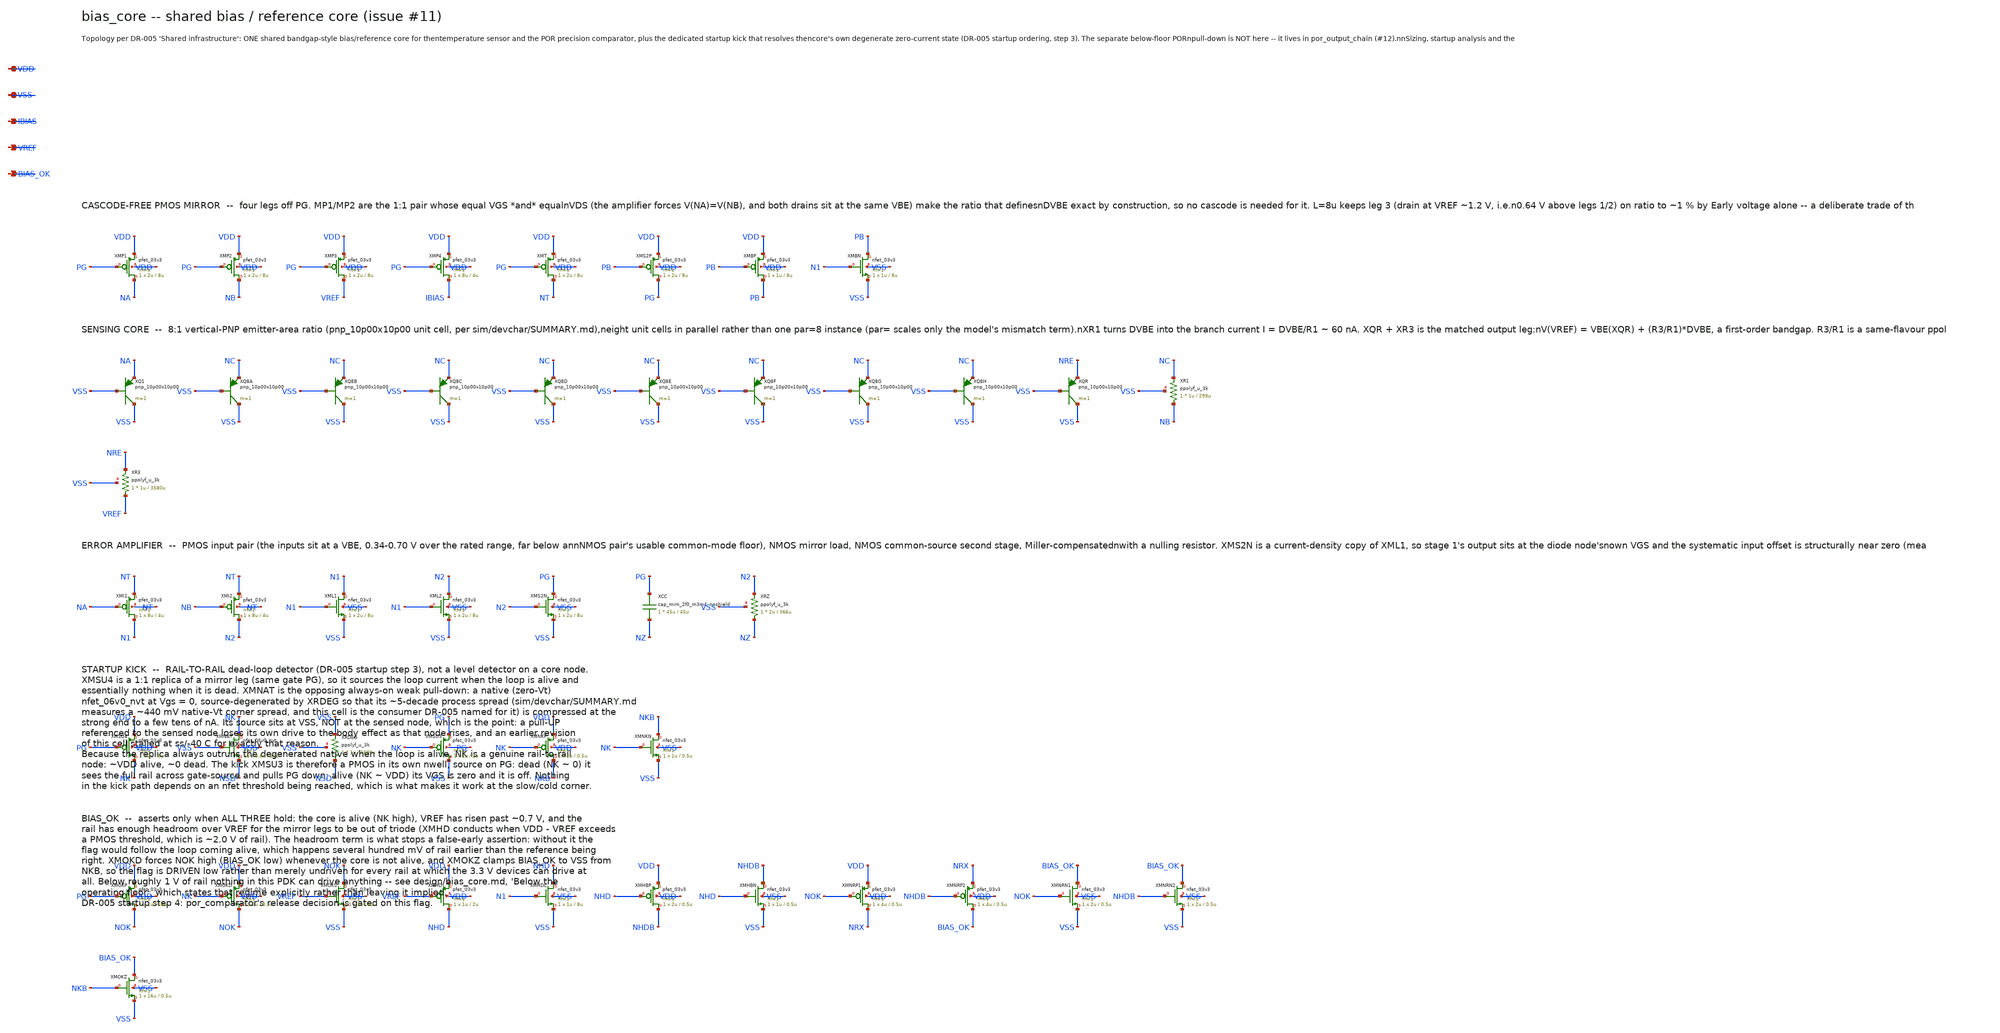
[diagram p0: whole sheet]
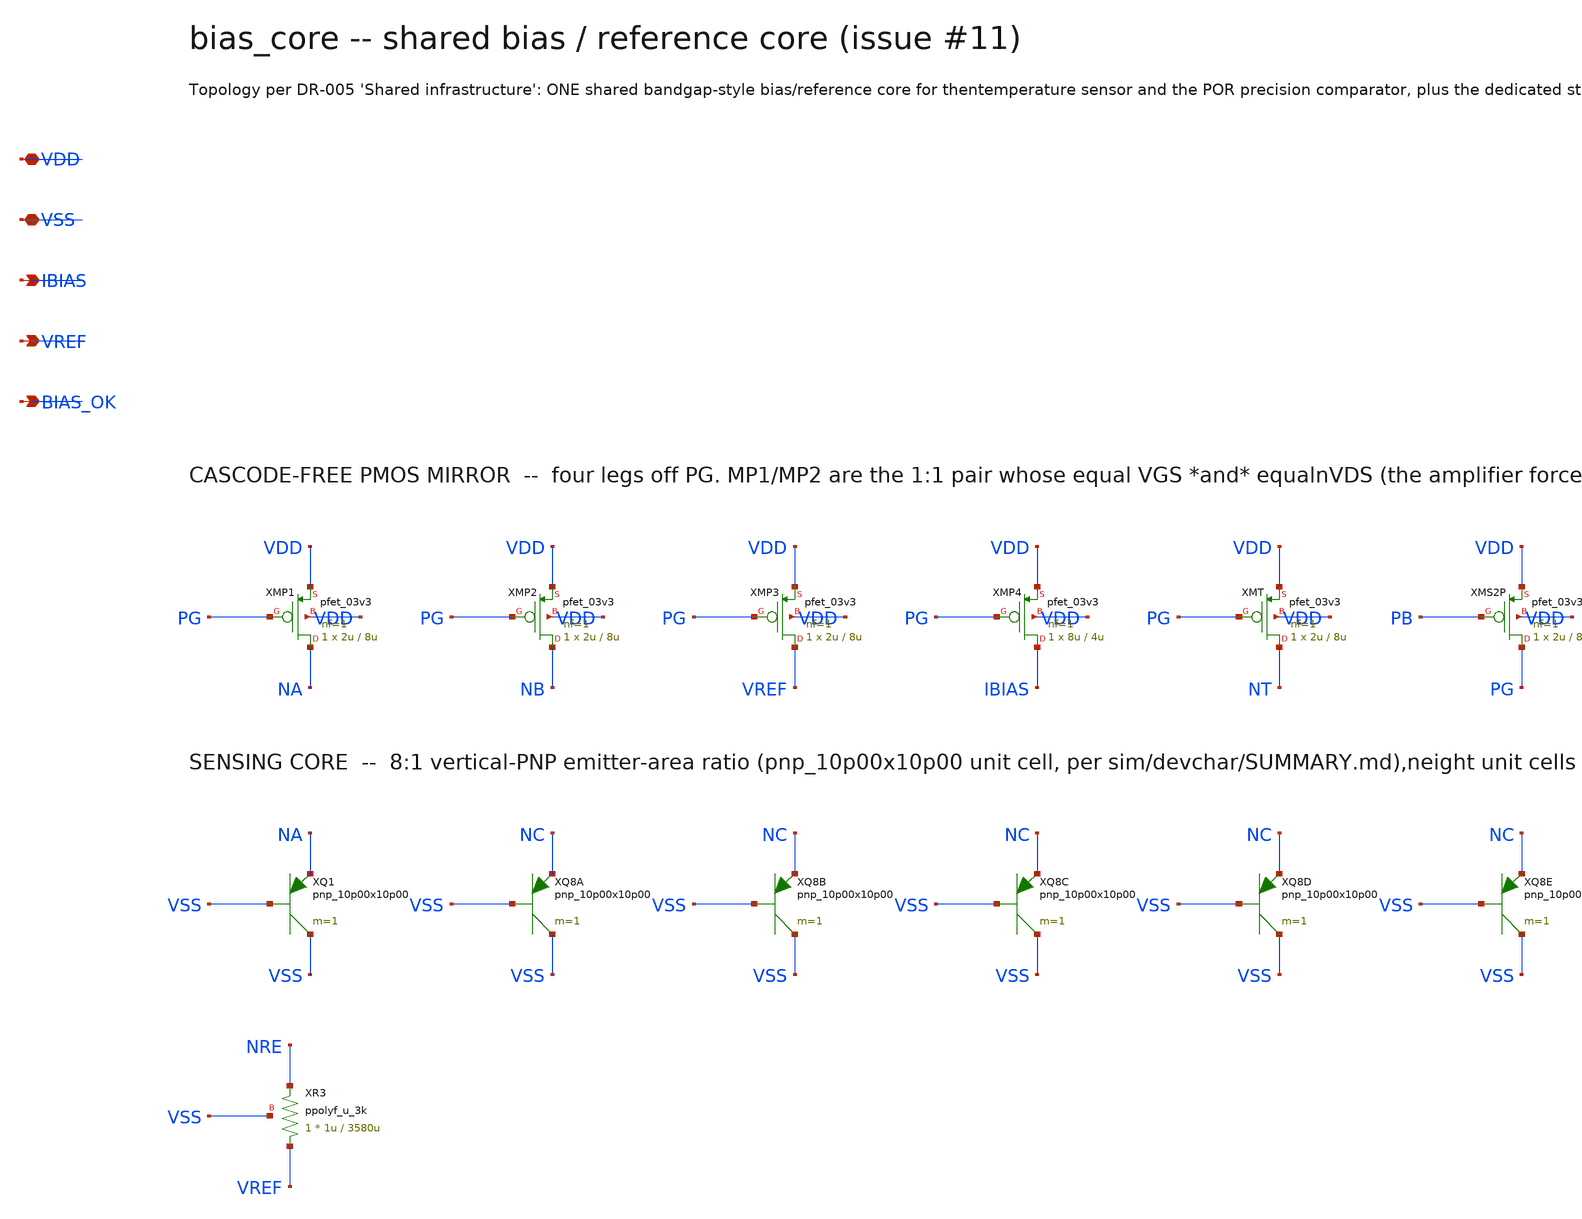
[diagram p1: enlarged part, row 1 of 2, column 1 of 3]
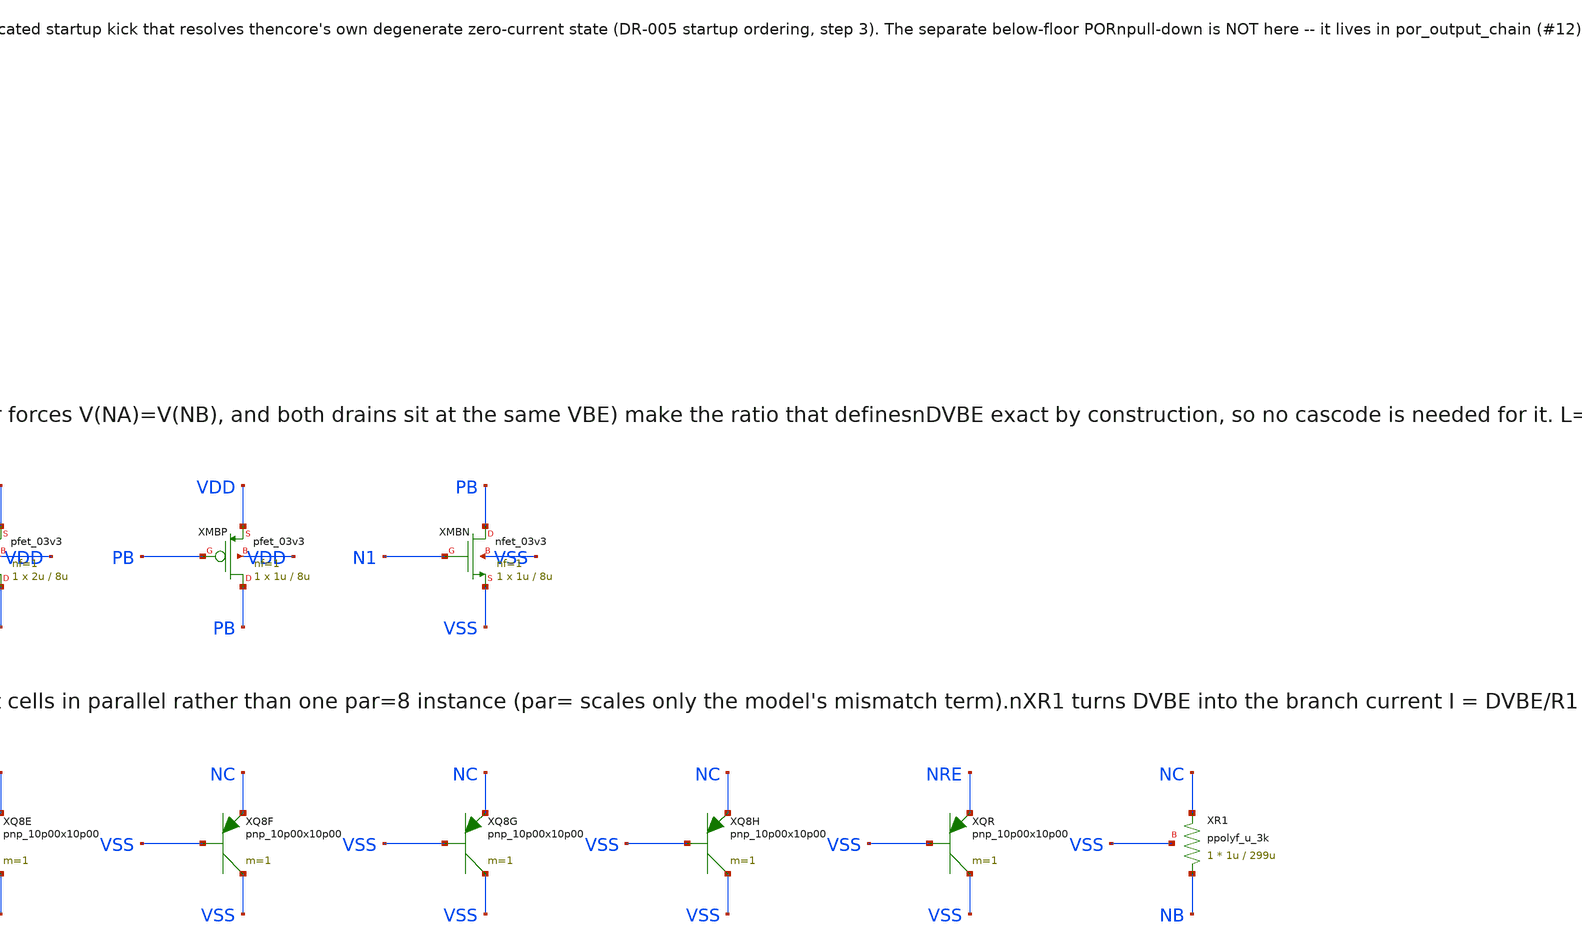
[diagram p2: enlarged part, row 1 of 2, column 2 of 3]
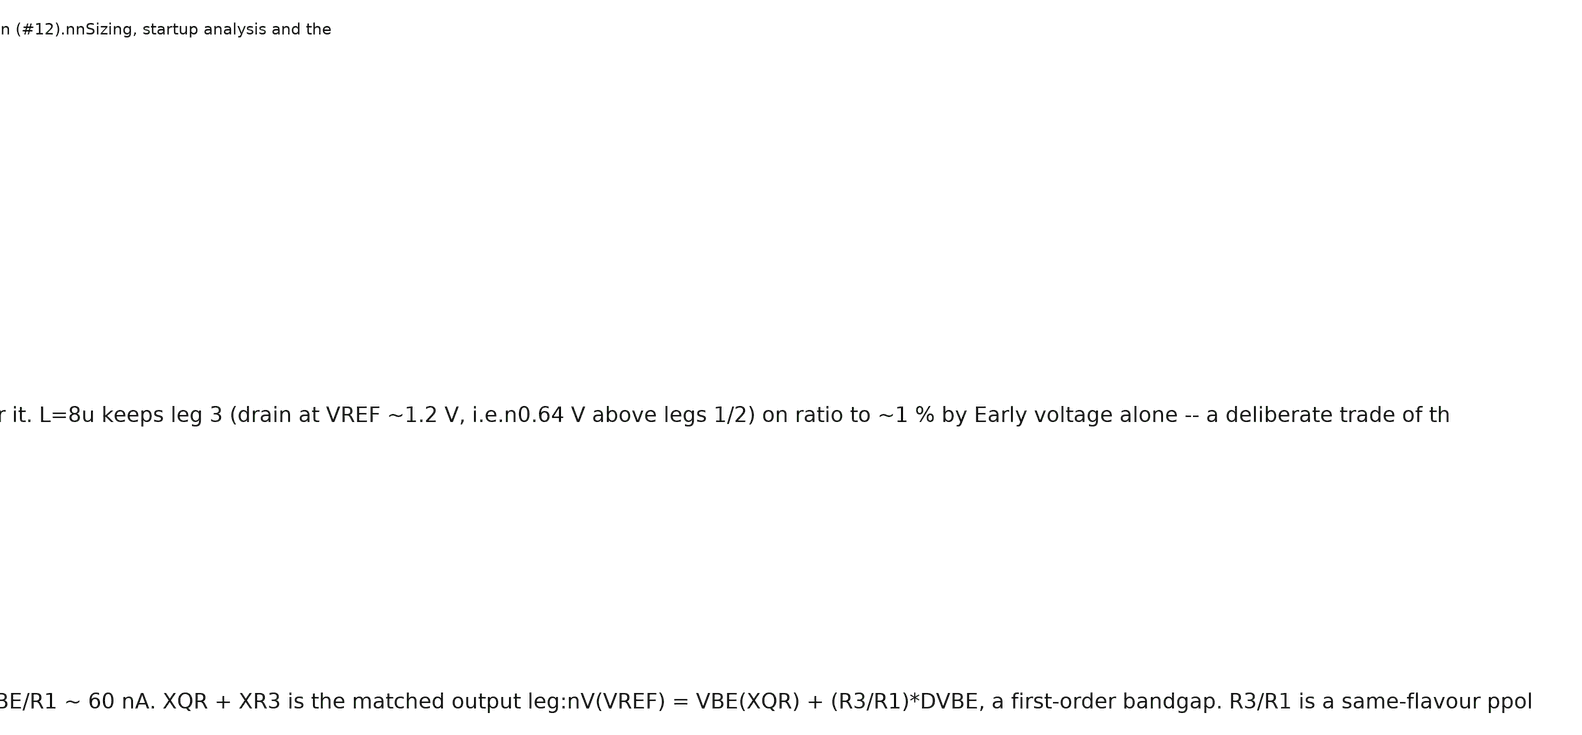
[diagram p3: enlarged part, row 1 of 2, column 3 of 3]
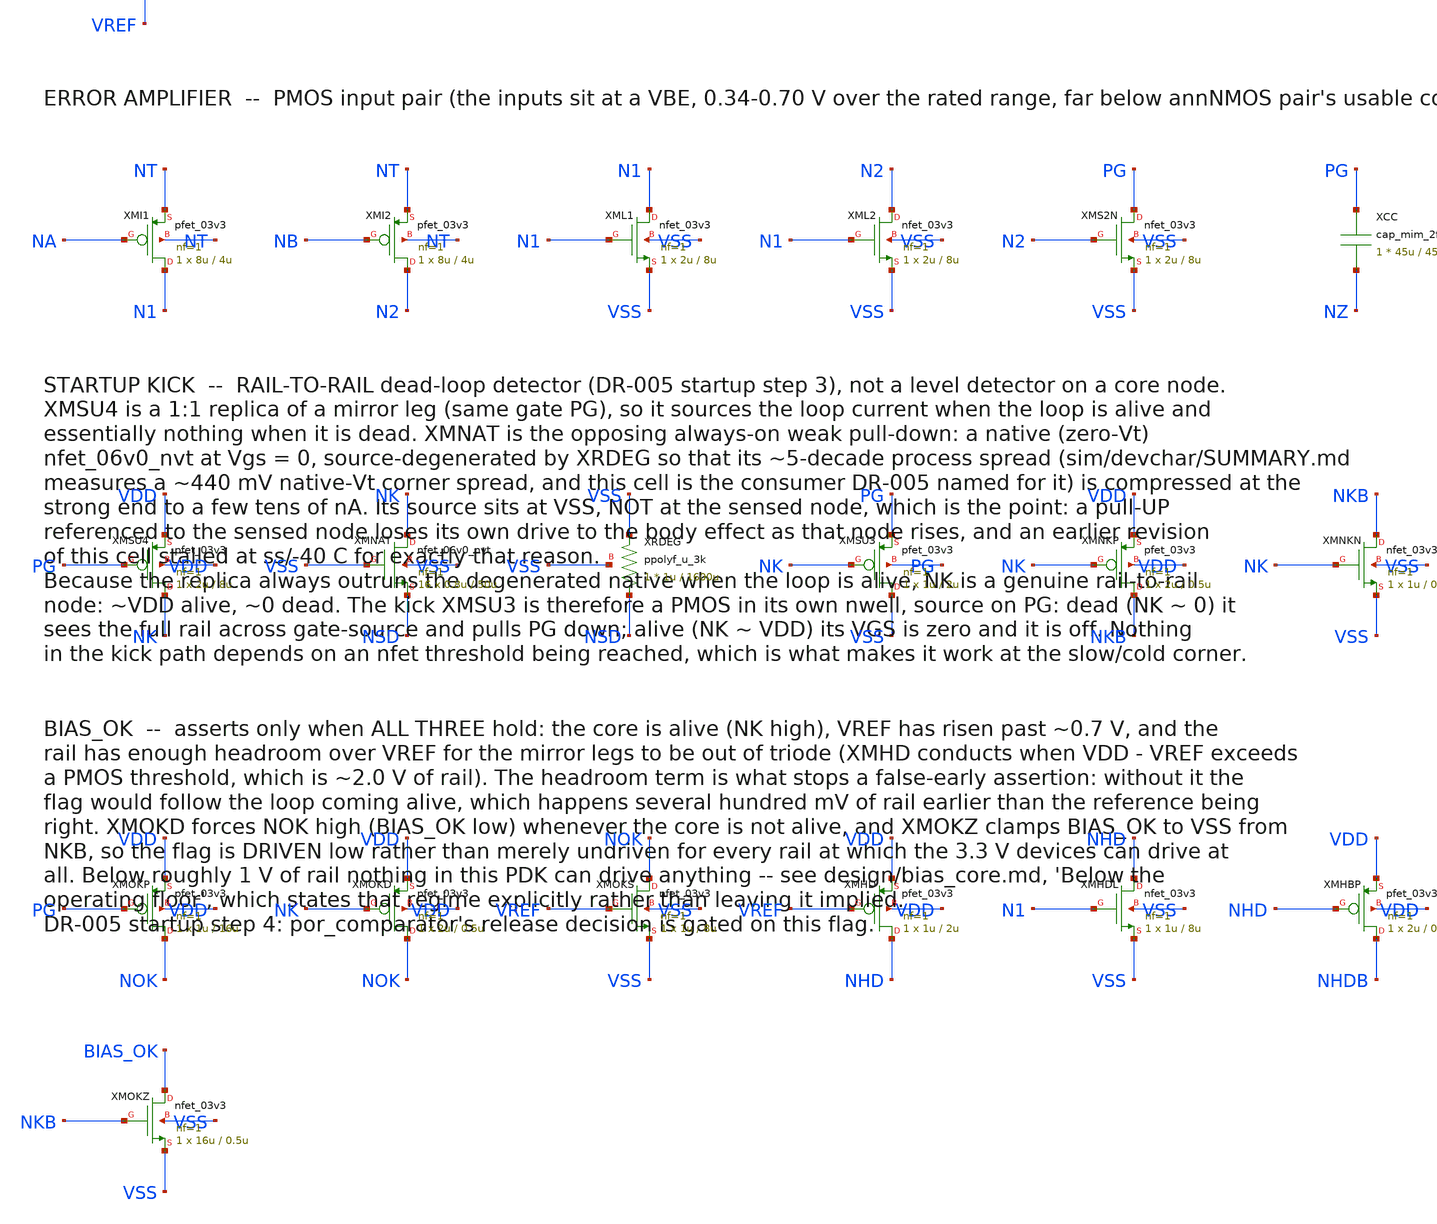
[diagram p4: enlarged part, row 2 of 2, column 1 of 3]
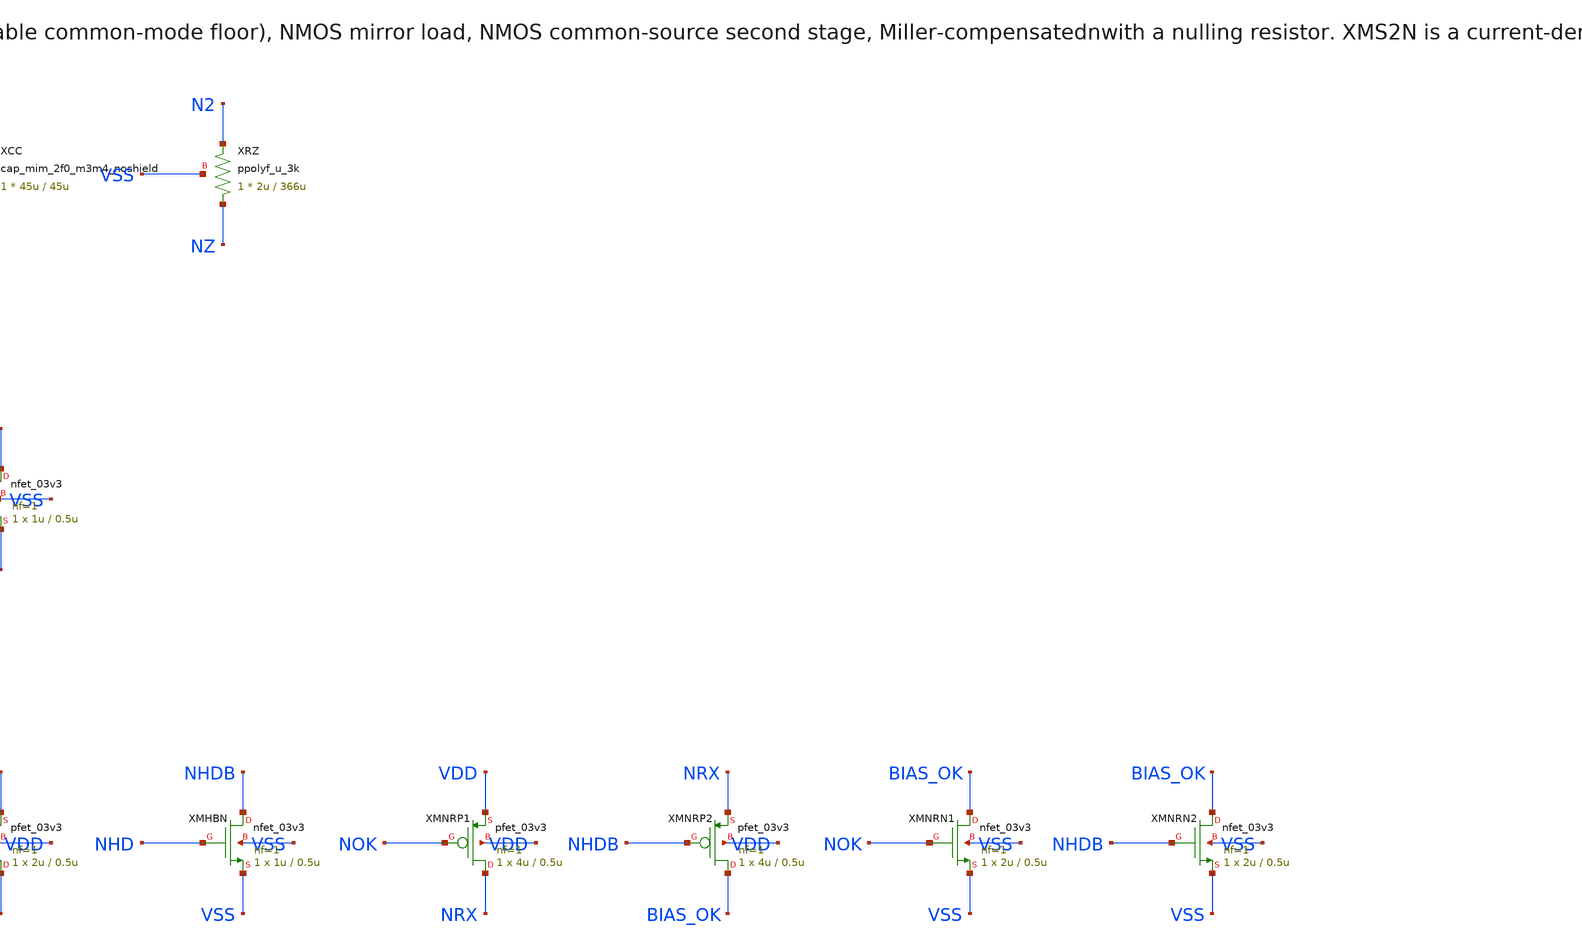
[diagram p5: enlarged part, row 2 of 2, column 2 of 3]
** sch_path: design/bias_core.sch
**.subckt bias_core VDD VSS IBIAS VREF BIAS_OK
*.iopin VDD
*.iopin VSS
*.opin IBIAS
*.opin VREF
*.opin BIAS_OK
XMP1 NA PG VDD VDD pfet_03v3 L=8u W=2u nf=1 ad='int((nf+1)/2) * W/nf * 0.18u' as='int((nf+2)/2) * W/nf * 0.18u'
+ pd='2*int((nf+1)/2) * (W/nf + 0.18u)' ps='2*int((nf+2)/2) * (W/nf + 0.18u)' nrd='0.18u / W' nrs='0.18u / W'
+ sa=0 sb=0 sd=0 m=1
XMP2 NB PG VDD VDD pfet_03v3 L=8u W=2u nf=1 ad='int((nf+1)/2) * W/nf * 0.18u' as='int((nf+2)/2) * W/nf * 0.18u'
+ pd='2*int((nf+1)/2) * (W/nf + 0.18u)' ps='2*int((nf+2)/2) * (W/nf + 0.18u)' nrd='0.18u / W' nrs='0.18u / W'
+ sa=0 sb=0 sd=0 m=1
XMP3 VREF PG VDD VDD pfet_03v3 L=8u W=2u nf=1 ad='int((nf+1)/2) * W/nf * 0.18u' as='int((nf+2)/2) * W/nf * 0.18u'
+ pd='2*int((nf+1)/2) * (W/nf + 0.18u)' ps='2*int((nf+2)/2) * (W/nf + 0.18u)' nrd='0.18u / W' nrs='0.18u / W'
+ sa=0 sb=0 sd=0 m=1
XMP4 IBIAS PG VDD VDD pfet_03v3 L=4u W=8u nf=1 ad='int((nf+1)/2) * W/nf * 0.18u' as='int((nf+2)/2) * W/nf * 0.18u'
+ pd='2*int((nf+1)/2) * (W/nf + 0.18u)' ps='2*int((nf+2)/2) * (W/nf + 0.18u)' nrd='0.18u / W' nrs='0.18u / W'
+ sa=0 sb=0 sd=0 m=1
XMT NT PG VDD VDD pfet_03v3 L=8u W=2u nf=1 ad='int((nf+1)/2) * W/nf * 0.18u' as='int((nf+2)/2) * W/nf * 0.18u'
+ pd='2*int((nf+1)/2) * (W/nf + 0.18u)' ps='2*int((nf+2)/2) * (W/nf + 0.18u)' nrd='0.18u / W' nrs='0.18u / W'
+ sa=0 sb=0 sd=0 m=1
XMS2P PG PB VDD VDD pfet_03v3 L=8u W=2u nf=1 ad='int((nf+1)/2) * W/nf * 0.18u' as='int((nf+2)/2) * W/nf * 0.18u'
+ pd='2*int((nf+1)/2) * (W/nf + 0.18u)' ps='2*int((nf+2)/2) * (W/nf + 0.18u)' nrd='0.18u / W' nrs='0.18u / W'
+ sa=0 sb=0 sd=0 m=1
XMBP PB PB VDD VDD pfet_03v3 L=8u W=1u nf=1 ad='int((nf+1)/2) * W/nf * 0.18u' as='int((nf+2)/2) * W/nf * 0.18u'
+ pd='2*int((nf+1)/2) * (W/nf + 0.18u)' ps='2*int((nf+2)/2) * (W/nf + 0.18u)' nrd='0.18u / W' nrs='0.18u / W'
+ sa=0 sb=0 sd=0 m=1
XMBN PB N1 VSS VSS nfet_03v3 L=8u W=1u nf=1 ad='int((nf+1)/2) * W/nf * 0.18u' as='int((nf+2)/2) * W/nf * 0.18u'
+ pd='2*int((nf+1)/2) * (W/nf + 0.18u)' ps='2*int((nf+2)/2) * (W/nf + 0.18u)' nrd='0.18u / W' nrs='0.18u / W'
+ sa=0 sb=0 sd=0 m=1
XQ1 VSS VSS NA pnp_10p00x10p00 m=1
XQ8A VSS VSS NC pnp_10p00x10p00 m=1
XQ8B VSS VSS NC pnp_10p00x10p00 m=1
XQ8C VSS VSS NC pnp_10p00x10p00 m=1
XQ8D VSS VSS NC pnp_10p00x10p00 m=1
XQ8E VSS VSS NC pnp_10p00x10p00 m=1
XQ8F VSS VSS NC pnp_10p00x10p00 m=1
XQ8G VSS VSS NC pnp_10p00x10p00 m=1
XQ8H VSS VSS NC pnp_10p00x10p00 m=1
XQR VSS VSS NRE pnp_10p00x10p00 m=1
XR1 NB NC VSS ppolyf_u_3k r_width=1u r_length=299u m=1
XR3 VREF NRE VSS ppolyf_u_3k r_width=1u r_length=3580u m=1
XMI1 N1 NA NT NT pfet_03v3 L=4u W=8u nf=1 ad='int((nf+1)/2) * W/nf * 0.18u' as='int((nf+2)/2) * W/nf * 0.18u'
+ pd='2*int((nf+1)/2) * (W/nf + 0.18u)' ps='2*int((nf+2)/2) * (W/nf + 0.18u)' nrd='0.18u / W' nrs='0.18u / W'
+ sa=0 sb=0 sd=0 m=1
XMI2 N2 NB NT NT pfet_03v3 L=4u W=8u nf=1 ad='int((nf+1)/2) * W/nf * 0.18u' as='int((nf+2)/2) * W/nf * 0.18u'
+ pd='2*int((nf+1)/2) * (W/nf + 0.18u)' ps='2*int((nf+2)/2) * (W/nf + 0.18u)' nrd='0.18u / W' nrs='0.18u / W'
+ sa=0 sb=0 sd=0 m=1
XML1 N1 N1 VSS VSS nfet_03v3 L=8u W=2u nf=1 ad='int((nf+1)/2) * W/nf * 0.18u' as='int((nf+2)/2) * W/nf * 0.18u'
+ pd='2*int((nf+1)/2) * (W/nf + 0.18u)' ps='2*int((nf+2)/2) * (W/nf + 0.18u)' nrd='0.18u / W' nrs='0.18u / W'
+ sa=0 sb=0 sd=0 m=1
XML2 N2 N1 VSS VSS nfet_03v3 L=8u W=2u nf=1 ad='int((nf+1)/2) * W/nf * 0.18u' as='int((nf+2)/2) * W/nf * 0.18u'
+ pd='2*int((nf+1)/2) * (W/nf + 0.18u)' ps='2*int((nf+2)/2) * (W/nf + 0.18u)' nrd='0.18u / W' nrs='0.18u / W'
+ sa=0 sb=0 sd=0 m=1
XMS2N PG N2 VSS VSS nfet_03v3 L=8u W=2u nf=1 ad='int((nf+1)/2) * W/nf * 0.18u' as='int((nf+2)/2) * W/nf * 0.18u'
+ pd='2*int((nf+1)/2) * (W/nf + 0.18u)' ps='2*int((nf+2)/2) * (W/nf + 0.18u)' nrd='0.18u / W' nrs='0.18u / W'
+ sa=0 sb=0 sd=0 m=1
XCC PG NZ cap_mim_2f0_m3m4_noshield c_width=45u c_length=45u m=1
XRZ NZ N2 VSS ppolyf_u_3k r_width=2u r_length=366u m=1
XMSU4 NK PG VDD VDD pfet_03v3 L=8u W=2u nf=1 ad='int((nf+1)/2) * W/nf * 0.18u' as='int((nf+2)/2) * W/nf * 0.18u'
+ pd='2*int((nf+1)/2) * (W/nf + 0.18u)' ps='2*int((nf+2)/2) * (W/nf + 0.18u)' nrd='0.18u / W' nrs='0.18u / W'
+ sa=0 sb=0 sd=0 m=1
XMNAT NK VSS NSD VSS nfet_06v0_nvt L=50u W=0.8u nf=1 ad='int((nf+1)/2) * W/nf * 0.18u' as='int((nf+2)/2) * W/nf * 0.18u'
+ pd='2*int((nf+1)/2) * (W/nf + 0.18u)' ps='2*int((nf+2)/2) * (W/nf + 0.18u)' nrd='0.18u / W' nrs='0.18u / W'
+ sa=0 sb=0 sd=0 m=16
XRDEG NSD VSS VSS ppolyf_u_3k r_width=1u r_length=1600u m=1
XMSU3 VSS NK PG PG pfet_03v3 L=2u W=1u nf=1 ad='int((nf+1)/2) * W/nf * 0.18u' as='int((nf+2)/2) * W/nf * 0.18u'
+ pd='2*int((nf+1)/2) * (W/nf + 0.18u)' ps='2*int((nf+2)/2) * (W/nf + 0.18u)' nrd='0.18u / W' nrs='0.18u / W'
+ sa=0 sb=0 sd=0 m=1
XMNKP NKB NK VDD VDD pfet_03v3 L=0.5u W=2u nf=1 ad='int((nf+1)/2) * W/nf * 0.18u' as='int((nf+2)/2) * W/nf * 0.18u'
+ pd='2*int((nf+1)/2) * (W/nf + 0.18u)' ps='2*int((nf+2)/2) * (W/nf + 0.18u)' nrd='0.18u / W' nrs='0.18u / W'
+ sa=0 sb=0 sd=0 m=1
XMNKN NKB NK VSS VSS nfet_03v3 L=0.5u W=1u nf=1 ad='int((nf+1)/2) * W/nf * 0.18u' as='int((nf+2)/2) * W/nf * 0.18u'
+ pd='2*int((nf+1)/2) * (W/nf + 0.18u)' ps='2*int((nf+2)/2) * (W/nf + 0.18u)' nrd='0.18u / W' nrs='0.18u / W'
+ sa=0 sb=0 sd=0 m=1
XMOKP NOK PG VDD VDD pfet_03v3 L=16u W=1u nf=1 ad='int((nf+1)/2) * W/nf * 0.18u' as='int((nf+2)/2) * W/nf * 0.18u'
+ pd='2*int((nf+1)/2) * (W/nf + 0.18u)' ps='2*int((nf+2)/2) * (W/nf + 0.18u)' nrd='0.18u / W' nrs='0.18u / W'
+ sa=0 sb=0 sd=0 m=1
XMOKD NOK NK VDD VDD pfet_03v3 L=0.5u W=2u nf=1 ad='int((nf+1)/2) * W/nf * 0.18u' as='int((nf+2)/2) * W/nf * 0.18u'
+ pd='2*int((nf+1)/2) * (W/nf + 0.18u)' ps='2*int((nf+2)/2) * (W/nf + 0.18u)' nrd='0.18u / W' nrs='0.18u / W'
+ sa=0 sb=0 sd=0 m=1
XMOKS NOK VREF VSS VSS nfet_03v3 L=8u W=1u nf=1 ad='int((nf+1)/2) * W/nf * 0.18u' as='int((nf+2)/2) * W/nf * 0.18u'
+ pd='2*int((nf+1)/2) * (W/nf + 0.18u)' ps='2*int((nf+2)/2) * (W/nf + 0.18u)' nrd='0.18u / W' nrs='0.18u / W'
+ sa=0 sb=0 sd=0 m=1
XMHD NHD VREF VDD VDD pfet_03v3 L=2u W=1u nf=1 ad='int((nf+1)/2) * W/nf * 0.18u' as='int((nf+2)/2) * W/nf * 0.18u'
+ pd='2*int((nf+1)/2) * (W/nf + 0.18u)' ps='2*int((nf+2)/2) * (W/nf + 0.18u)' nrd='0.18u / W' nrs='0.18u / W'
+ sa=0 sb=0 sd=0 m=1
XMHDL NHD N1 VSS VSS nfet_03v3 L=8u W=1u nf=1 ad='int((nf+1)/2) * W/nf * 0.18u' as='int((nf+2)/2) * W/nf * 0.18u'
+ pd='2*int((nf+1)/2) * (W/nf + 0.18u)' ps='2*int((nf+2)/2) * (W/nf + 0.18u)' nrd='0.18u / W' nrs='0.18u / W'
+ sa=0 sb=0 sd=0 m=1
XMHBP NHDB NHD VDD VDD pfet_03v3 L=0.5u W=2u nf=1 ad='int((nf+1)/2) * W/nf * 0.18u' as='int((nf+2)/2) * W/nf * 0.18u'
+ pd='2*int((nf+1)/2) * (W/nf + 0.18u)' ps='2*int((nf+2)/2) * (W/nf + 0.18u)' nrd='0.18u / W' nrs='0.18u / W'
+ sa=0 sb=0 sd=0 m=1
XMHBN NHDB NHD VSS VSS nfet_03v3 L=0.5u W=1u nf=1 ad='int((nf+1)/2) * W/nf * 0.18u' as='int((nf+2)/2) * W/nf * 0.18u'
+ pd='2*int((nf+1)/2) * (W/nf + 0.18u)' ps='2*int((nf+2)/2) * (W/nf + 0.18u)' nrd='0.18u / W' nrs='0.18u / W'
+ sa=0 sb=0 sd=0 m=1
XMNRP1 NRX NOK VDD VDD pfet_03v3 L=0.5u W=4u nf=1 ad='int((nf+1)/2) * W/nf * 0.18u' as='int((nf+2)/2) * W/nf * 0.18u'
+ pd='2*int((nf+1)/2) * (W/nf + 0.18u)' ps='2*int((nf+2)/2) * (W/nf + 0.18u)' nrd='0.18u / W' nrs='0.18u / W'
+ sa=0 sb=0 sd=0 m=1
XMNRP2 BIAS_OK NHDB NRX VDD pfet_03v3 L=0.5u W=4u nf=1 ad='int((nf+1)/2) * W/nf * 0.18u' as='int((nf+2)/2) * W/nf * 0.18u'
+ pd='2*int((nf+1)/2) * (W/nf + 0.18u)' ps='2*int((nf+2)/2) * (W/nf + 0.18u)' nrd='0.18u / W' nrs='0.18u / W'
+ sa=0 sb=0 sd=0 m=1
XMNRN1 BIAS_OK NOK VSS VSS nfet_03v3 L=0.5u W=2u nf=1 ad='int((nf+1)/2) * W/nf * 0.18u' as='int((nf+2)/2) * W/nf * 0.18u'
+ pd='2*int((nf+1)/2) * (W/nf + 0.18u)' ps='2*int((nf+2)/2) * (W/nf + 0.18u)' nrd='0.18u / W' nrs='0.18u / W'
+ sa=0 sb=0 sd=0 m=1
XMNRN2 BIAS_OK NHDB VSS VSS nfet_03v3 L=0.5u W=2u nf=1 ad='int((nf+1)/2) * W/nf * 0.18u' as='int((nf+2)/2) * W/nf * 0.18u'
+ pd='2*int((nf+1)/2) * (W/nf + 0.18u)' ps='2*int((nf+2)/2) * (W/nf + 0.18u)' nrd='0.18u / W' nrs='0.18u / W'
+ sa=0 sb=0 sd=0 m=1
XMOKZ BIAS_OK NKB VSS VSS nfet_03v3 L=0.5u W=16u nf=1 ad='int((nf+1)/2) * W/nf * 0.18u' as='int((nf+2)/2) * W/nf * 0.18u'
+ pd='2*int((nf+1)/2) * (W/nf + 0.18u)' ps='2*int((nf+2)/2) * (W/nf + 0.18u)' nrd='0.18u / W' nrs='0.18u / W'
+ sa=0 sb=0 sd=0 m=1
**.ends
.end
